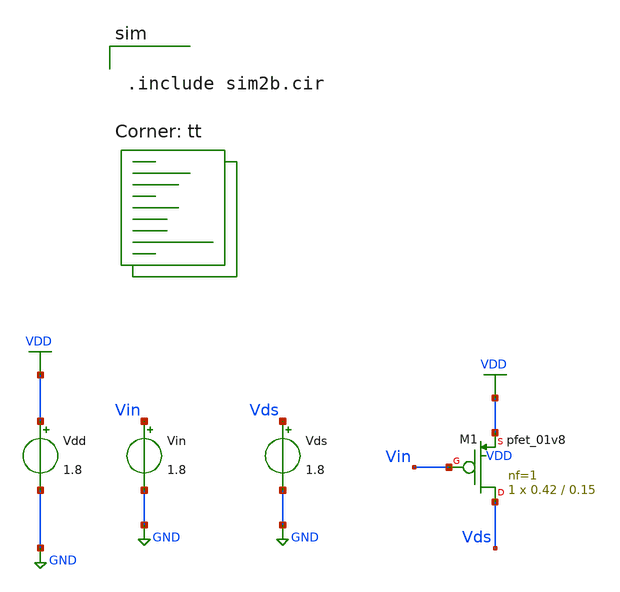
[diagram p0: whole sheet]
** sch_path: assignments/assignment1/assign2b.sch
**.subckt assign2b
Vdd VDD GND 1.8
XM1 Vds Vin VDD VDD sky130_fd_pr__pfet_01v8 L=0.15 W=0.42 nf=1 ad='int((nf+1)/2) * W/nf * 0.29' as='int((nf+2)/2) * W/nf * 0.29'
+ pd='2*int((nf+1)/2) * (W/nf + 0.29)' ps='2*int((nf+2)/2) * (W/nf + 0.29)' nrd='0.29 / W' nrs='0.29 / W'
+ sa=0 sb=0 sd=0 mult=1 m=1
Vin Vin GND 1.8
Vds Vds GND 1.8
**** begin user architecture code


.include sim2b.cir


.lib $::SKYWATER_MODELS/sky130.lib.spice tt
**** end user architecture code
**.ends
.GLOBAL GND
.GLOBAL VDD
.end
